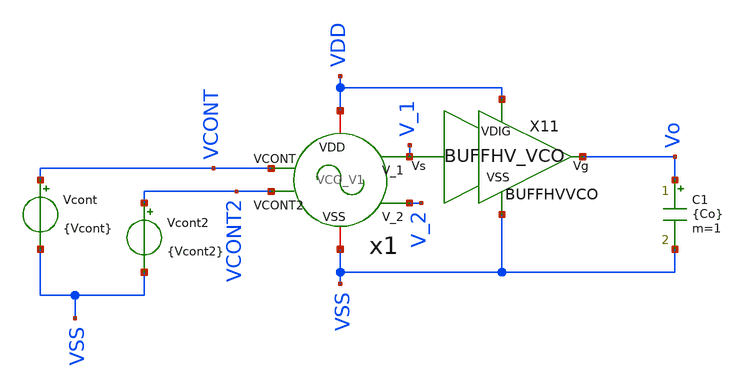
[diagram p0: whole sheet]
** sch_path: xschem/VCO/TB_VCO_V1.sch
**.subckt TB_VCO_V1
C1 Vo VSS {Co} m=1
Vcont VCONT VSS {Vcont}
Vcont2 VCONT2 VSS {Vcont2}
x1 VCONT VSS VDD V_1 V_2 VCONT2 VCO_V1
X11 V_1 Vo VDD VSS BUFFHVVCO
**** begin user architecture code

.param Co = 1p
.param mult = 1
.param w_inv = 0.15u
.param l_inv = 0.15u

.param Vcont = 1
.param VCP = 0.57
.param VCN = 0.76

vvdd vdd 0 dc 3.3
vvss vss 0 0
*vvcont VCONT 0 dc 0
*vvcont2 VCONT2 0 dc 0
*.option temp = 200
.ic v(V_1) = 0
.ic v(V_2) = 3.3
*.ic v(V_11) = 0
*.ic v(V_22) = 3.3
.save v(V_1) v(Vo)

*.param fmin = 60Meg
*.param fmin = 15Meg
*.param fmin = 10Meg
*.param fmin = 7.5Meg
*.param fmin = 4Meg
.param fmin = 2Meg
*.param fmin = 1.62Meg
*.param fmin = 1Meg
*.param fmin = 0.7Meg
*.param fmin = 0.4Meg
.param Tmin = 1/fmin
.param SimTime =  Tmin*20
.csparam SimTime ={Simtime}
.csparam Tmargin = Tmin*2





.lib cornerMOShv.lib mos_tt
.lib cornerMOSlv.lib mos_tt
*.lib cornerMOShv.lib mos_ff
*.lib cornerMOSlv.lib mos_ff
*.lib cornerMOShv.lib mos_ss
*.lib cornerMOSlv.lib mos_ss
*.lib cornerMOShv.lib mos_sf
*.lib cornerMOSlv.lib mos_sf
*.lib cornerMOShv.lib mos_fs
*.lib cornerMOSlv.lib mos_fs

*.include /opt/pdks/ihp-sg13g2/libs.ref/sg13g2_stdcell/spice/sg13g2_stdcell.spice
*.lib $::SG13G2_MODELS/cornerRES.lib res_typ
*.lib $::SG13G2_MODELS/cornerCAP.lib cap_typ
*.lib $::SG13G2_MODELS/diodes.lib




.option KLU
*.option itl4=100
.option method=gear
*.option maxord=2
*.option trtol=25
*.option lvltim=1
*.option tnum=1e9
*.option reltol=1e-3
*.option abstol=1e-10
*.option vntol=1e-4
*.option event
*.option gmin=1e-10
*.option cshunt=1e-13




.param Vcont2 = 1.8

.param w_MP1a =1u
.param l_MP1a = 8u
.param w_MP1b = 3u
.param l_MP1b = 8u
.param w_MP2 = 7u
.param l_MP2 = 1u
.param w_MP3 = 8u
.param l_MP3 = 1u
.param w_MP4 = 2u
.param l_MP4 = 10u

.param w_MN1 = 2u
.param l_MN1 = 1u
.param w_MN2 = 1u
.param l_MN2 = 1u
.param w_MN3 = 2u
.param l_MN3 = 1u
.param w_MN4 = 0.5u
.param l_MN4 = 10u

.param m_MP1a = 1
.param m_MP1b = 1
.param m_MP2 = 1
.param m_MP3 = 1
.param m_MP4 = 1
.param m_MN1 = 1
.param m_MN2 = 1
.param m_MN3 = 1
.param m_MN4 = 1



.save all
.param Vcont = 1

.control
reset
unset filetype
op
alter Vcont 1
let VCN = v(x1.x1.VCN)
let VCP = v(x1.x1.VCP)

let Vsd_MP4 = v(x1.x1.VSMP4) - v(x1.x1.VOUT)
let Vsd_MP3 = v(VDD) - v(x1.x1.VSMP4)
let Vsd_MP2 = v(VDD) - v(x1.x1.VCP)
let Vsd_MP1 = v(VDD) - VCN
let Vds_MN4 = v(x1.x1.VOUT) - v(x1.x1.VdsMN3)

let Vth_MP1a = @n.x1.x1.xmp1a.nsg13_hv_pmos[vth]
let Vth_MP1b = @n.x1.x1.xmp1b.nsg13_hv_pmos[vth]
let Vth_MP2 = @n.x1.x1.xmp2.nsg13_hv_pmos[vth]
let Vth_MP3 = @n.x1.x1.xmp3.nsg13_hv_pmos[vth]
let Vth_MP4 = @n.x1.x1.xmp3.nsg13_hv_pmos[vth]
let Vth_MN1 = @n.x1.x1.xmn1.nsg13_hv_nmos[vth]
let Vth_MN2 = @n.x1.x1.xmn2.nsg13_hv_nmos[vth]
let Vth_MN3 = @n.x1.x1.xmn3.nsg13_hv_nmos[vth]
let Vth_MN4 = @n.x1.x1.xmn4.nsg13_hv_nmos[vth]

let Vsg_MP4 = v(x1.x1.VSMP4) - v(x1.x1.VIN)
let Vsg_MP3 = v(VDD) - VCP
let Vsg_MP1a = v(VDD) - v(VCONT)
let Vsg_MP1b = v(VDD) - v(VCONT2)
let Vgs_MN4 = v(x1.x1.VIN) - v(x1.x1.VdsMN3)

let Vov_MP1a = Vsg_MP1a - Vth_MP1a
let Vov_MP1b = Vsg_MP1b - Vth_MP1b
let Vov_MP3 = Vsg_MP3 - Vth_MP3
let Vov_MP4 = Vsg_MP4 - Vth_MP4
let Vov_MN2 =  VCN - Vth_MN2
let Vov_MN3 =  VCN - Vth_MN3
let Vov_MN4 =  VCN - Vth_MN4

let gds_MN3 = @n.x1.x1.xmn3.nsg13_hv_nmos[gds]
let Ron_MN3 = 1/gds_MN3
let gds_MP3 = @n.x1.x1.xmp3.nsg13_hv_pmos[gds]
let Ron_MP3 = 1/gds_MP3
let M_P = gds_MP3/Vov_MP3
let M_N = gds_MN3/Vov_MN3


write TB_VCO_V1.raw
.endc





.save all


.csparam start = 10
.param Vcont = 1

.control

dc VdMP1 0 3.3 0.2 VgMP1 0 3.3 0.2
let IdMP1a = i(VIcont)
let IdMP1a_Diode = i(VIcont1)
let  VsdMP1 = v(Vdd) - v(VdMP1)
let VthMP1 = @n.xMP1.msky130_fd_pr__pfet_01v8[vth]
let  VovMP1a = v(Vdd) - v(VdMP1) - VthMP1
*plot IdMP1a IdMP1a_Diode vs VsdMP1
*plot IdMP1a_Diode vs VovMP1

let IdMP1b = i(VIcont4)
let IdMP1b_Diode = i(VIcont5)
let  VsdMP1 = v(Vdd) - v(VdMP1)
let VthMP1 = @n.xMP1.msky130_fd_pr__pfet_01v8[vth]
let  VovMP1b = v(Vdd) - v(VdMP1) - VthMP1
*plot IdMP1b IdMP1b_Diode vs VsdMP1
*plot IdMP1b_Diode vs VovMP1

let IdMP2 = i(VIcont2)
let IdMP2_Diode = i(VIcont3)
let  VsdMP2 = v(Vdd) - v(VdMP2)
let VthMP2 = @m.xMP4.msky130_fd_pr__pfet_01v8[vth]
let  VovMP2 = v(Vdd) - v(VdMP2) - VthMP2
*plot IdMP2 IdMP2_Diode vs VsdMP2
*plot IdMP2_Diode vs VovMP2
let KP1 = IdMP1_Diode/(VovMP1*VovMP1)
let AP1 = sqrt(KP1)
let KP2 = IdMP2_Diode/(VovMP2*VovMP2)
let AP2 = sqrt(KP2)

plot AP1 AP2

*plot IdMP1_Diode IdMP2_Diode vs VsdMP1
print VthMP1 VthMP2
*wrdata ../../sim_data/data_VCO_design.txt IdMP1_Diode VovMP1 IdMP1 vs VsdMP1
wrdata
+ /workspaces/usm-vlsi-tools/shared_xserver/simulations/SKY130/IPD500-TimebasedDCDCBuck/sim_data/data_VCO_design.txt IdMP1_Diode VovMP1 IdMP1 vs VsdMP1
wrdata
+ /workspaces/usm-vlsi-tools/shared_xserver/simulations/SKY130/IPD500-TimebasedDCDCBuck/sim_data/data_AP1_VthMP1.txt AP1 VthMP1 AP2 VthMP2

reset
*load save_data.raw
*show

dc VdMN1 0 3.3 0.2 VgMN1 0 3.3 0.2
let VdsMN1 = v(VdsMN1)
let IdMN1_Diode = i(VIdMN1)
let IdMN1 = i(VIdMN2)
let VthMN1 = @m.xMN1.msky130_fd_pr__nfet_01v8[vth]
let VovMN1 = VdsMN1 - VthMN1
*plot IdMN1 IdMN1_Diode vs VdsMN1
*plot IdMN1_Diode vs VovMN1

let VdsMN2 = v(VdsMN1)
let IdMN2_Diode = i(VIdMN3)
let IdMN2 = i(VIdMN4)
let VthMN2 = @m.xMN4.msky130_fd_pr__nfet_01v8[vth]
let VovMN2 = VdsMN2 - VthMN2
*plot IdMN2 IdMN2_Diode vs VdsMN2
*plot IdMN2_Diode vs VovMN2

let KN1 = IdMN1_Diode/(VovMN1*VovMN1)
let AN1 = sqrt(KN1)
let KN2 = IdMN2_Diode/(VovMN2*VovMN2)
let AN2 = sqrt(KN2)
*plot AN1 AN2
print VthMN1 VthMN2
wrdata
+ /workspaces/usm-vlsi-tools/shared_xserver/simulations/SKY130/IPD500-TimebasedDCDCBuck/sim_data/data_AN1_VthMN1.txt AN1 VthMN1


reset

dc Vcont 0 2 0.1
*dc Vcont 0 3 0.1


let Icont = i(v.x1.x1.VIcont)
let Icont2 = i(v.x1.x1.VIcont1)
let Icont3 = i(v.x1.x1.VIcont3)
let VCN = v(x1.x1.VCN)
let VCP = v(x1.x1.VCP)
let Vsg_MP3 = v(Vdd) - VCP
let VsdMP3 = v(VDD) - v(x1.x1.VSMP4)
let VdsMN3 = v(x1.x1.VdsMN3)

let Vth_MP3 = @n.x1.x1.xmp3.nsg13_hv_pmos[vth]
let Vth_MN3 = @n.x1.x1.xmn3.nsg13_hv_nmos[vth]

let Vsg_MP3 = v(VDD) - VCP

let Vov_MP3 = Vsg_MP3 - Vth_MP3
let Vov_MN3 =  VCN - Vth_MN3

let gds_MN3 = @n.x1.x1.xmn3.nsg13_hv_nmos[gds]
let Ron_MN3 = 1/gds_MN3
let gds_MP3 = @n.x1.x1.xmp3.nsg13_hv_pmos[gds]
let Ron_MP3 = 1/gds_MP3
let M_P = gds_MP3/Vov_MP3
let M_N = gds_MN3/Vov_MN3

plot M_P M_N vs Vcont
plot Icont Icont2 Icont3 vs Vcont
plot Icont3 vs Vcont
plot Icont3 vs VCP
plot VCP vs Vcont
plot VCN Vsg_MP3 vs Vcont
plot VsdMP3 VdsMN3 vs Vcont
*plot Vin vs Vcont
.endc



**** end user architecture code
**.ends

* expanding   symbol:  ../VCO/VCO_V1.sym # of pins=6
** sym_path: xschem/VCO/VCO_V1.sym
** sch_path: xschem/VCO/VCO_V1.sch
.subckt VCO_V1 VCONT VSS VDD V_1 V_2 VCONT2
*.ipin VCONT
*.iopin VDD
*.iopin VSS
*.opin V_1
*.opin V_2
*.ipin VCONT2
x1 VDD VCONT V_1 V_5 VSS VCONT2 stage_V1
x2 VDD VCONT V_2 V_1 VSS VCONT2 stage_V1
x3 VDD VCONT V_3 V_2 VSS VCONT2 stage_V1
x4 VDD VCONT V_4 V_3 VSS VCONT2 stage_V1
x5 VDD VCONT V_5 V_4 VSS VCONT2 stage_V1
.ends


* expanding   symbol:  ../BUFFHVVCO/BUFFHVVCO.sym # of pins=4
** sym_path: xschem/BUFFHVVCO/BUFFHVVCO.sym
** sch_path: xschem/BUFFHVVCO/BUFFHVVCO.sch
.subckt BUFFHVVCO Vs Vg VDIG VSS
*.iopin VDIG
*.ipin Vs
*.opin Vg
*.iopin VSS
XMD5 net1 Vs VDIG VDIG sg13_hv_pmos w=1u l=0.45u ng=1 m=2 mm_ok=1
XMD6 VSS Vs net1 VSS sg13_hv_nmos w=1u l=0.45u ng=1 m=1 mm_ok=1
XMD1 Vg net1 VDIG VDIG sg13_hv_pmos w=1u l=0.45u ng=1 m=4 mm_ok=1
XMD2 VSS net1 Vg VSS sg13_hv_nmos w=1u l=0.45u ng=1 m=2 mm_ok=1
.ends


* expanding   symbol:  ../VCO/stage_V1.sym # of pins=6
** sym_path: xschem/VCO/stage_V1.sym
** sch_path: xschem/VCO/stage_V1.sch
.subckt stage_V1 VDD VCONT VOUT VIN VSS VCONT2
*.ipin VCONT2
*.ipin VIN
*.opin VOUT
*.iopin VDD
*.iopin VSS
*.ipin VCONT
XMN1 VSS net2 net2 VSS sg13_hv_nmos w={w_MN1} l={l_MN1} ng=1 m={m_MN1} mm_ok=1
XMN2 VSS net2 net3 VSS sg13_hv_nmos w={w_MN2} l={l_MN2} ng=1 m={m_MN2} mm_ok=1
XMN3 VSS net2 VdsMN3 VSS sg13_hv_nmos w={w_MN3} l={l_MN3} ng=1 m={m_MN3} mm_ok=1
XMP1a VCN VCONT VDD VDD sg13_hv_pmos w={w_MP1a} l={l_MP1a} ng=1 m={m_MP1a} mm_ok=1
XMP2 VCP VCP VDD VDD sg13_hv_pmos w={w_MP2} l={l_MP2} ng=1 m={m_MP2} mm_ok=1
XMP3 net4 VCP VDD VDD sg13_hv_pmos w={w_MP3} l={l_MP3} ng=1 m={m_MP3} mm_ok=1
XMP7 net1 VIN VSMP4 VDD sg13_hv_pmos w={w_MP4} l={l_MP4} ng=1 m={m_MP4} mm_ok=1
XMN4 VdsMN3 VIN net1 VSS sg13_hv_nmos w={w_MN4} l={l_MN4} ng=1 m={m_MN4} mm_ok=1
XMP1b VCN VCONT2 VDD VDD sg13_hv_pmos w={w_MP1b} l={l_MP1b} ng=1 m={m_MP1b} mm_ok=1
VIcont1 VCN net2 0
.save i(vicont1)
VIcont2 VCP net3 0
.save i(vicont2)
VIcont3 net4 VSMP4 0
.save i(vicont3)
VIcont4 net1 VOUT 0
.save i(vicont4)
.ends

.end
